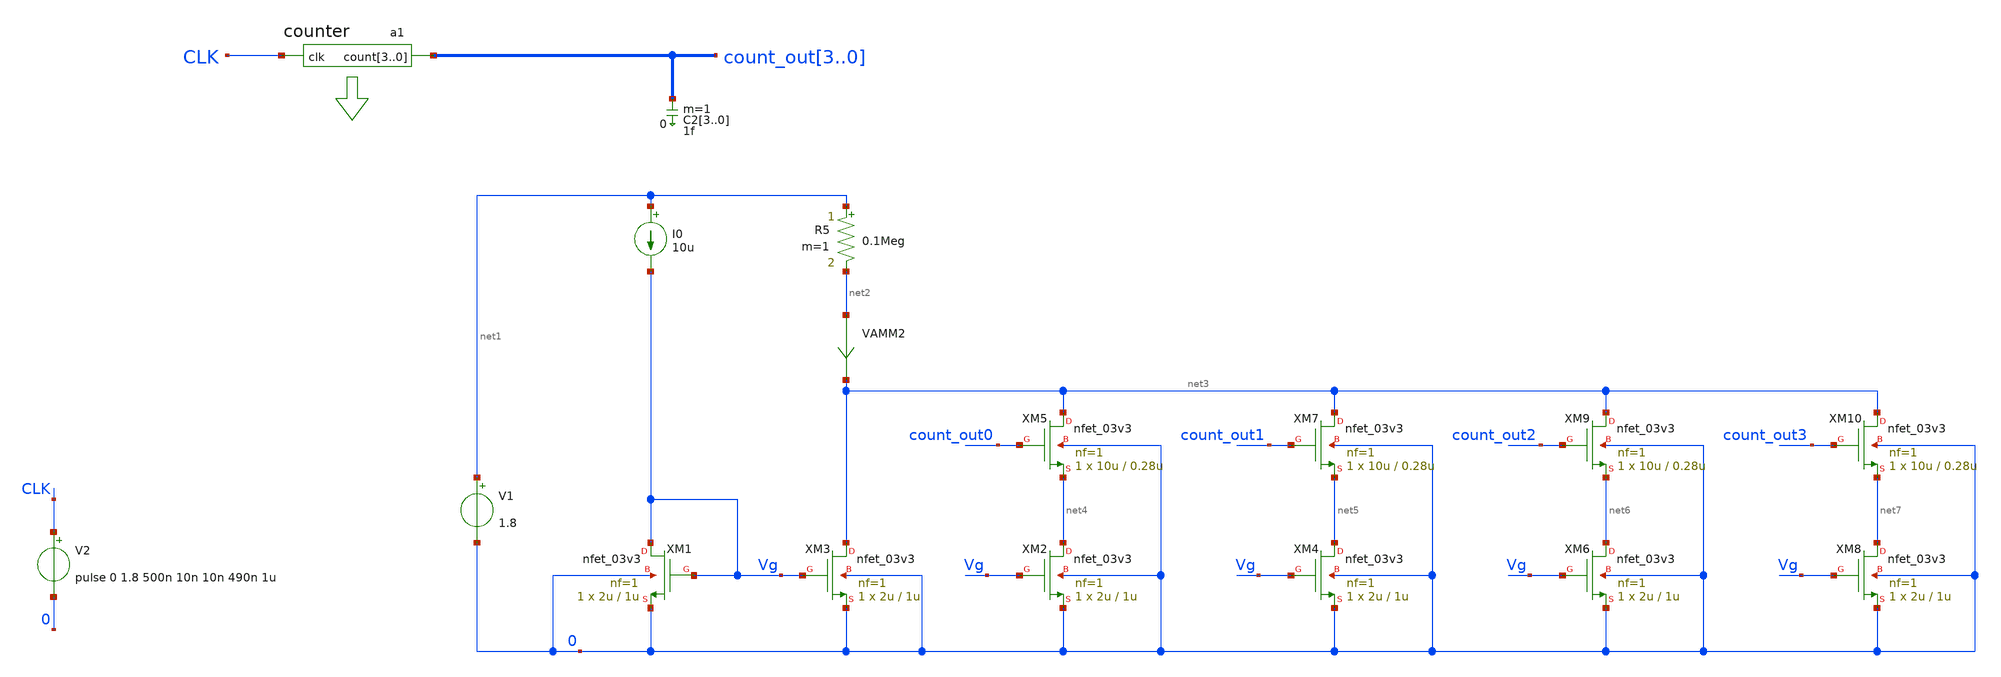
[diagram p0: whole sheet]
** sch_path: resources/C_MOSbius_playground_for_chips/cosimulation/schematic_view/cosimulation/current_mirror_cosim.sch
**.subckt current_mirror_cosim
C23 count_out3 0 1f m=1
C22 count_out2 0 1f m=1
C21 count_out1 0 1f m=1
C20 count_out0 0 1f m=1
a1 [ CLK ] [ count_out3 count_out2 count_out1 count_out0 ] counter
V2 CLK 0 pulse 0 1.8 500n 10n 10n 490n 1u
I0 net1 Vg 10u
V1 net1 0 1.8
R5 net1 net2 0.1Meg m=1
VAMM2 net2 net3 0
XM3 net3 Vg 0 0 nfet_03v3 L=1u W=2u nf=1 ad='int((nf+1)/2) * W/nf * 0.18u' as='int((nf+2)/2) * W/nf * 0.18u'
+ pd='2*int((nf+1)/2) * (W/nf + 0.18u)' ps='2*int((nf+2)/2) * (W/nf + 0.18u)' nrd='0.18u / W' nrs='0.18u / W'
+ sa=0 sb=0 sd=0 m=1
XM1 Vg Vg 0 0 nfet_03v3 L=1u W=2u nf=1 ad='int((nf+1)/2) * W/nf * 0.18u' as='int((nf+2)/2) * W/nf * 0.18u'
+ pd='2*int((nf+1)/2) * (W/nf + 0.18u)' ps='2*int((nf+2)/2) * (W/nf + 0.18u)' nrd='0.18u / W' nrs='0.18u / W'
+ sa=0 sb=0 sd=0 m=1
XM2 net4 Vg 0 0 nfet_03v3 L=1u W=2u nf=1 ad='int((nf+1)/2) * W/nf * 0.18u' as='int((nf+2)/2) * W/nf * 0.18u'
+ pd='2*int((nf+1)/2) * (W/nf + 0.18u)' ps='2*int((nf+2)/2) * (W/nf + 0.18u)' nrd='0.18u / W' nrs='0.18u / W'
+ sa=0 sb=0 sd=0 m=1
XM4 net5 Vg 0 0 nfet_03v3 L=1u W=2u nf=1 ad='int((nf+1)/2) * W/nf * 0.18u' as='int((nf+2)/2) * W/nf * 0.18u'
+ pd='2*int((nf+1)/2) * (W/nf + 0.18u)' ps='2*int((nf+2)/2) * (W/nf + 0.18u)' nrd='0.18u / W' nrs='0.18u / W'
+ sa=0 sb=0 sd=0 m=1
XM6 net6 Vg 0 0 nfet_03v3 L=1u W=2u nf=1 ad='int((nf+1)/2) * W/nf * 0.18u' as='int((nf+2)/2) * W/nf * 0.18u'
+ pd='2*int((nf+1)/2) * (W/nf + 0.18u)' ps='2*int((nf+2)/2) * (W/nf + 0.18u)' nrd='0.18u / W' nrs='0.18u / W'
+ sa=0 sb=0 sd=0 m=1
XM8 net7 Vg 0 0 nfet_03v3 L=1u W=2u nf=1 ad='int((nf+1)/2) * W/nf * 0.18u' as='int((nf+2)/2) * W/nf * 0.18u'
+ pd='2*int((nf+1)/2) * (W/nf + 0.18u)' ps='2*int((nf+2)/2) * (W/nf + 0.18u)' nrd='0.18u / W' nrs='0.18u / W'
+ sa=0 sb=0 sd=0 m=1
XM5 net3 count_out0 net4 0 nfet_03v3 L=0.28u W=10u nf=1 ad='int((nf+1)/2) * W/nf * 0.18u' as='int((nf+2)/2) * W/nf * 0.18u'
+ pd='2*int((nf+1)/2) * (W/nf + 0.18u)' ps='2*int((nf+2)/2) * (W/nf + 0.18u)' nrd='0.18u / W' nrs='0.18u / W'
+ sa=0 sb=0 sd=0 m=1
XM7 net3 count_out1 net5 0 nfet_03v3 L=0.28u W=10u nf=1 ad='int((nf+1)/2) * W/nf * 0.18u' as='int((nf+2)/2) * W/nf * 0.18u'
+ pd='2*int((nf+1)/2) * (W/nf + 0.18u)' ps='2*int((nf+2)/2) * (W/nf + 0.18u)' nrd='0.18u / W' nrs='0.18u / W'
+ sa=0 sb=0 sd=0 m=1
XM9 net3 count_out2 net6 0 nfet_03v3 L=0.28u W=10u nf=1 ad='int((nf+1)/2) * W/nf * 0.18u' as='int((nf+2)/2) * W/nf * 0.18u'
+ pd='2*int((nf+1)/2) * (W/nf + 0.18u)' ps='2*int((nf+2)/2) * (W/nf + 0.18u)' nrd='0.18u / W' nrs='0.18u / W'
+ sa=0 sb=0 sd=0 m=1
XM10 net3 count_out3 net7 0 nfet_03v3 L=0.28u W=10u nf=1 ad='int((nf+1)/2) * W/nf * 0.18u' as='int((nf+2)/2) * W/nf * 0.18u'
+ pd='2*int((nf+1)/2) * (W/nf + 0.18u)' ps='2*int((nf+2)/2) * (W/nf + 0.18u)' nrd='0.18u / W' nrs='0.18u / W'
+ sa=0 sb=0 sd=0 m=1
**** begin user architecture code


.temp 27

.option method=gear

.control
save all
tran 0.1n 50u
*set wr_singlescale
*set wr_vecnames
*option numdgt=4
*plot i(Vmeas) i(Vmeas1)
remzerovec
write current_mirror_cosim.raw

.endc



.include $::180MCU_MODELS/design.ngspice
.lib $::180MCU_MODELS/sm141064.ngspice typical

**** end user architecture code
**.ends
**** begin user architecture code
.model counter d_cosim simulation="ivlng" sim_args=["counter"] delay=0
**** end user architecture code
.end
